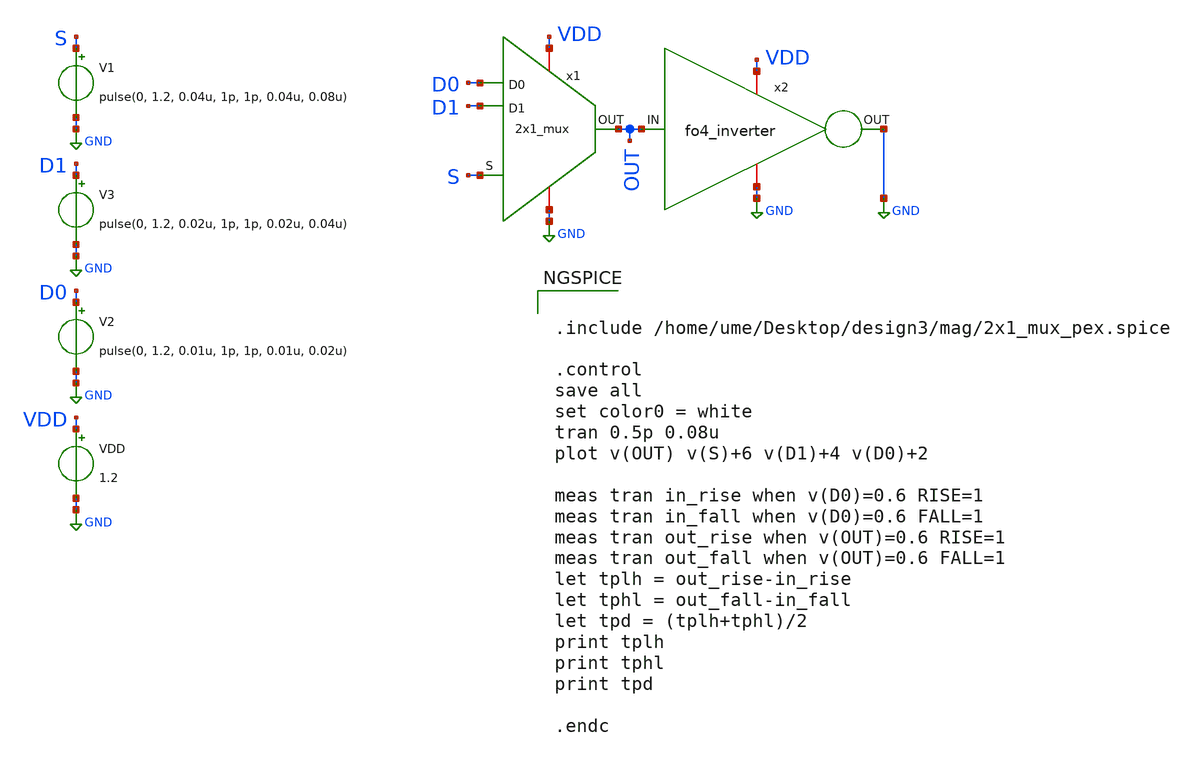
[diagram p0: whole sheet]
** sch_path: design/2x1_mux_with_fo4/2x1_mux_tb.sch
**.subckt 2x1_mux_tb
V1 S GND pulse(0, 1.2, 0.04u, 1p, 1p, 0.04u, 0.08u)
V2 D0 GND pulse(0, 1.2, 0.01u, 1p, 1p, 0.01u, 0.02u)
V3 D1 GND pulse(0, 1.2, 0.02u, 1p, 1p, 0.02u, 0.04u)
VDD VDD GND 1.2
x2 VDD OUT GND GND fo4_inverter
x1 GND VDD S D0 D1 OUT 2x1_mux
**** begin user architecture code

** opencircuitdesign pdks install
.lib $::SKYWATER_MODELS/sky130.lib.spice tt_mm




.include /home/ume/Desktop/design3/mag/2x1_mux_pex.spice

.control
save all
set color0 = white
tran 0.5p 0.08u
plot v(OUT) v(S)+6 v(D1)+4 v(D0)+2

meas tran in_rise when v(D0)=0.6 RISE=1
meas tran in_fall when v(D0)=0.6 FALL=1
meas tran out_rise when v(OUT)=0.6 RISE=1
meas tran out_fall when v(OUT)=0.6 FALL=1
let tplh = out_rise-in_rise
let tphl = out_fall-in_fall
let tpd = (tplh+tphl)/2
print tplh
print tphl
print tpd

.endc

**** end user architecture code
**.ends

* expanding   symbol:  inv_with_fo4/fo4_inverter.sym # of pins=4
** sym_path: design/2x1_mux_with_fo4/fo4_inverter.sym
** sch_path: design/2x1_mux_with_fo4/fo4_inverter.sch
.subckt fo4_inverter VDD IN OUT VSS
*.ipin IN
*.iopin VDD
*.iopin VSS
*.opin OUT
x1 VDD OUT IN VSS inverter
x2 VDD OUT IN VSS inverter
x3 VDD OUT IN VSS inverter
x4 VDD OUT IN VSS inverter
.ends


* expanding   symbol:  inverter.sym # of pins=4
** sym_path: design/ALU/inverter.sym
** sch_path: design/ALU/inverter.sch
.subckt inverter VDD OUT IN VSS
*.ipin IN
*.iopin VDD
*.opin OUT
*.iopin VSS
XM2 OUT IN VDD VDD sky130_fd_pr__pfet_01v8 L=0.15 W=0.9 nf=1 ad='int((nf+1)/2) * W/nf * 0.29' as='int((nf+2)/2) * W/nf * 0.29'
+ pd='2*int((nf+1)/2) * (W/nf + 0.29)' ps='2*int((nf+2)/2) * (W/nf + 0.29)' nrd='0.29 / W' nrs='0.29 / W'
+ sa=0 sb=0 sd=0 mult=1 m=1
XM1 OUT IN VSS VSS sky130_fd_pr__nfet_01v8 L=0.15 W=0.42 nf=1 ad='int((1 + 1)/2) * 0.42 / 1 * 0.29' as='int((1 + 2)/2) * 0.42 / 1 * 0.29'
+ pd='2*int((1 + 1)/2) * (0.42 / 1 + 0.29)' ps='2*int((1 + 2)/2) * (0.42 / 1 + 0.29)' nrd='0.29 / 0.42 '
+ nrs='0.29 / 0.42 ' sa=0 sb=0 sd=0 mult=1 m=1
.ends

.GLOBAL GND
.end
